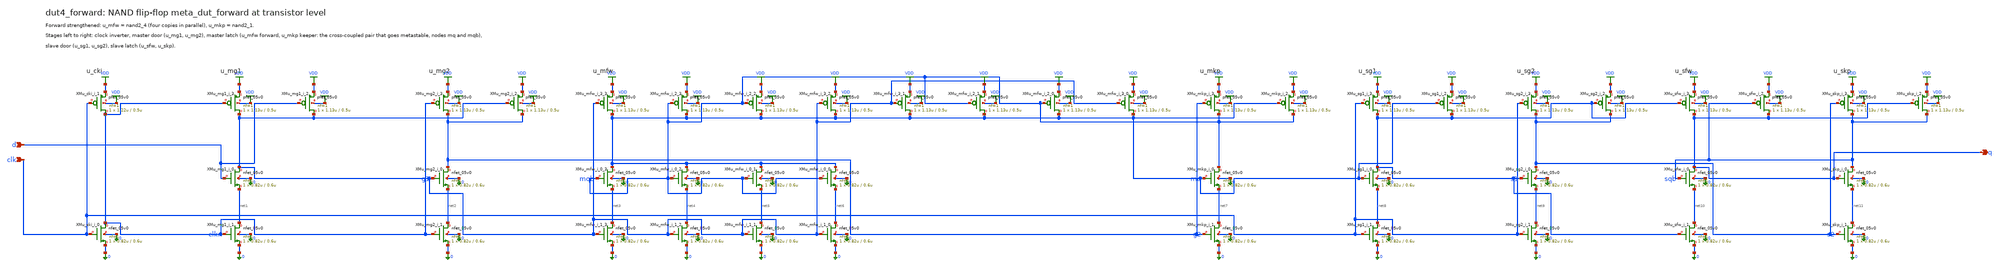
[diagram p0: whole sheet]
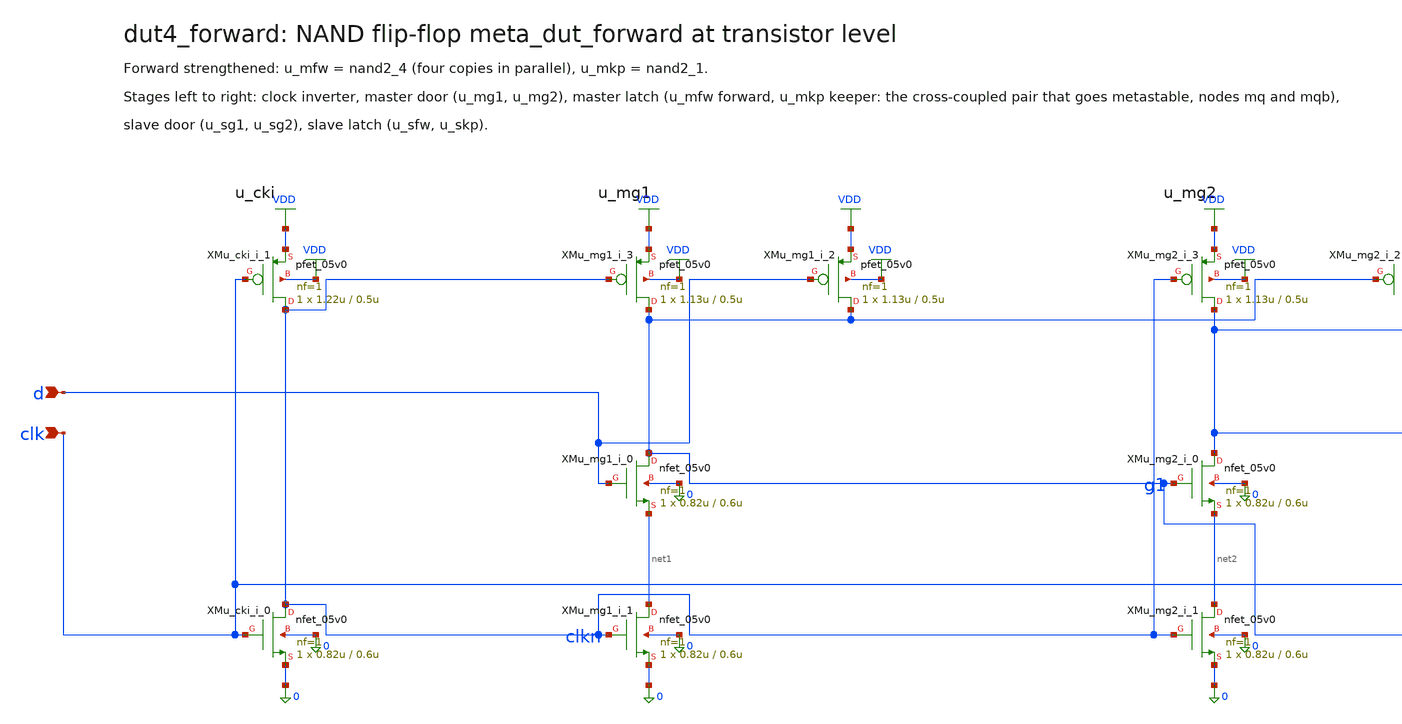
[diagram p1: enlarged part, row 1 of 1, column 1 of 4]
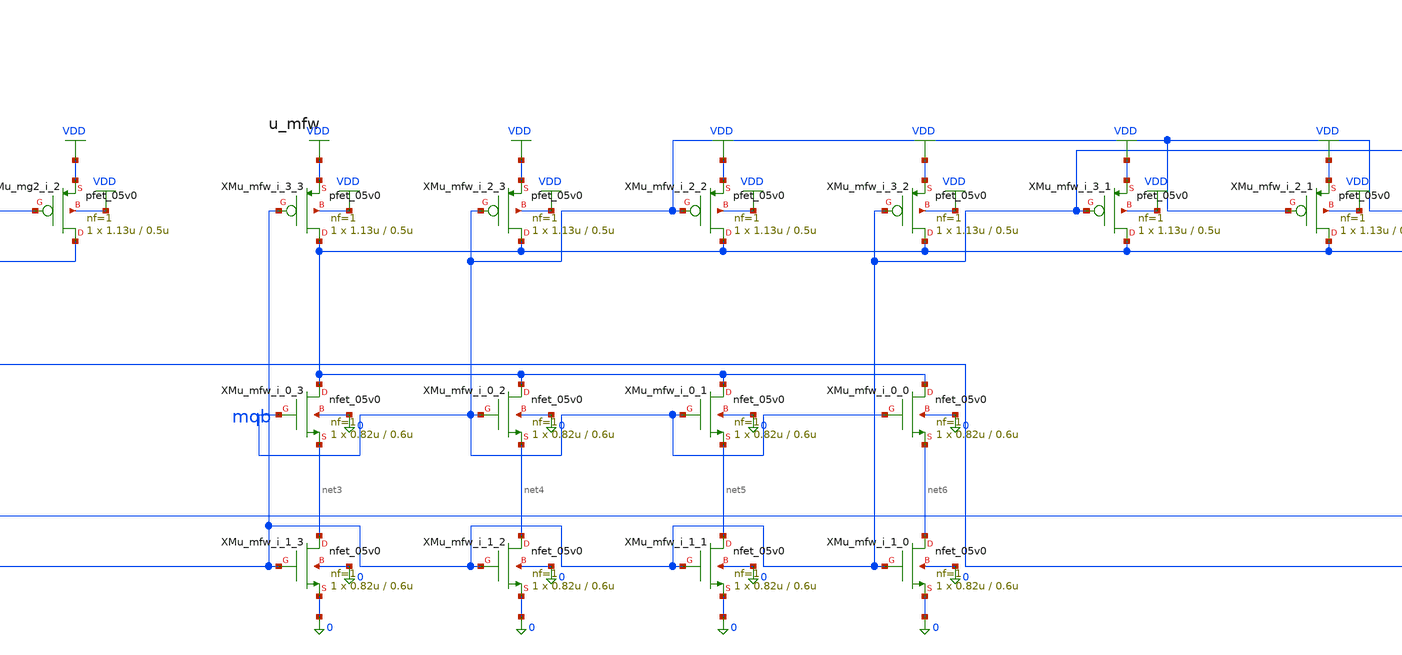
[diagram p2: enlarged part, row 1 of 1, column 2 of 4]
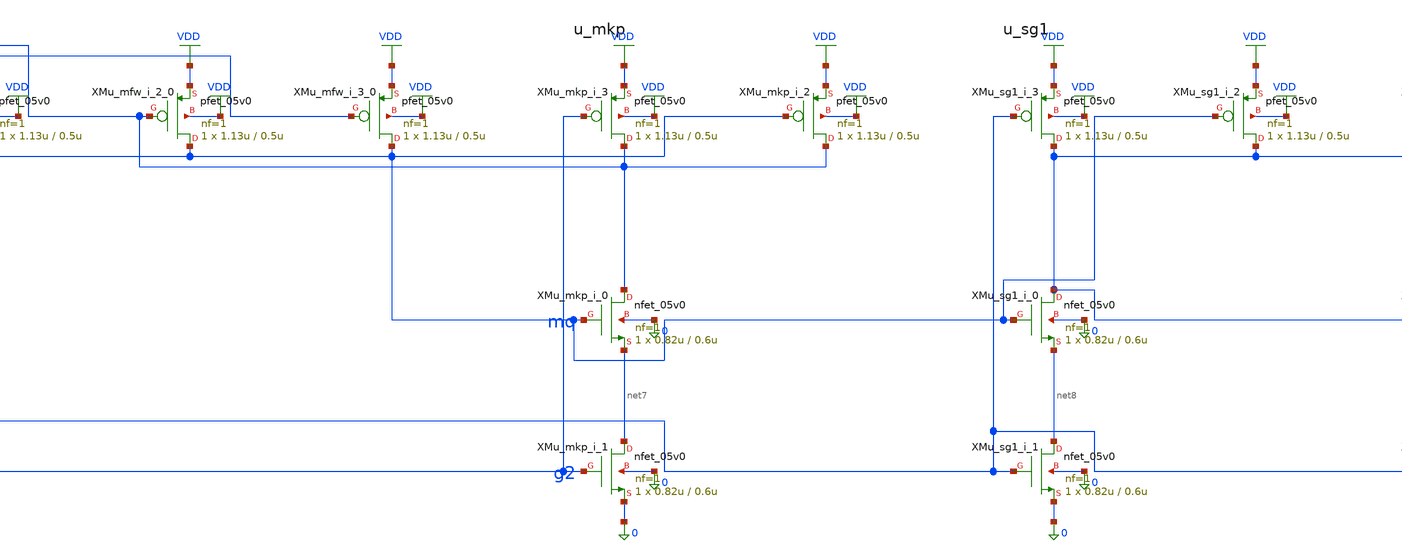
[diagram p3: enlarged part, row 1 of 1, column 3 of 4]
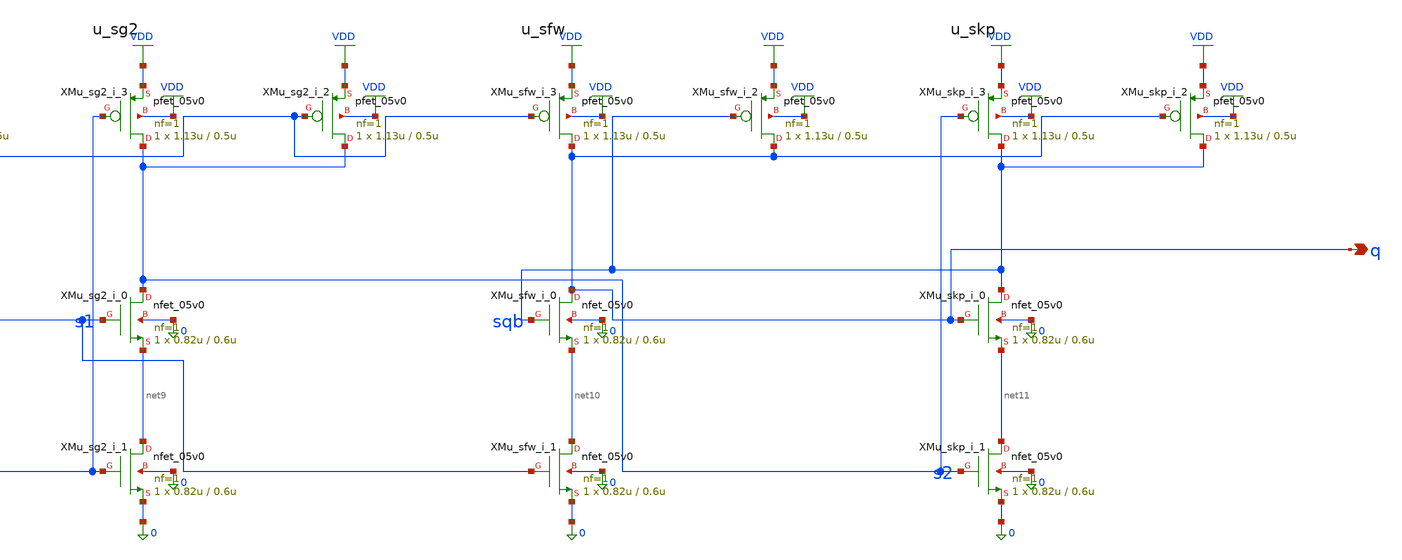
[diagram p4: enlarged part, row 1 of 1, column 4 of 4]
** sch_path: xschem/flat/dut4_forward.sch
**.subckt dut4_forward d clk q
*.ipin d
*.ipin clk
*.opin q
XMu_cki_i_0 clkn clk 0 0 nfet_05v0 L=0.6u W=0.82u nf=1 ad=4.1e-13 as=4.1e-13 pd=2.64e-06 ps=2.64e-06
+ nrd=0 nrs=0 sa=0 sb=0 sd=0 m=1
XMu_cki_i_1 clkn clk VDD VDD pfet_05v0 L=0.5u W=1.22u nf=1 ad=6.1e-13 as=6.1e-13 pd=3.44e-06
+ ps=3.44e-06 nrd=0 nrs=0 sa=0 sb=0 sd=0 m=1
XMu_mg1_i_1 net1 clkn 0 0 nfet_05v0 L=0.6u W=0.82u nf=1 ad=4.1e-13 as=4.1e-13 pd=2.64e-06
+ ps=2.64e-06 nrd=0 nrs=0 sa=0 sb=0 sd=0 m=1
XMu_mg1_i_0 g1 d net1 0 nfet_05v0 L=0.6u W=0.82u nf=1 ad=4.1e-13 as=4.1e-13 pd=2.64e-06 ps=2.64e-06
+ nrd=0 nrs=0 sa=0 sb=0 sd=0 m=1
XMu_mg1_i_3 g1 clkn VDD VDD pfet_05v0 L=0.5u W=1.13u nf=1 ad=5.65e-13 as=5.65e-13 pd=3.26e-06
+ ps=3.26e-06 nrd=0 nrs=0 sa=0 sb=0 sd=0 m=1
XMu_mg1_i_2 g1 d VDD VDD pfet_05v0 L=0.5u W=1.13u nf=1 ad=5.65e-13 as=5.65e-13 pd=3.26e-06
+ ps=3.26e-06 nrd=0 nrs=0 sa=0 sb=0 sd=0 m=1
XMu_mg2_i_1 net2 clkn 0 0 nfet_05v0 L=0.6u W=0.82u nf=1 ad=4.1e-13 as=4.1e-13 pd=2.64e-06
+ ps=2.64e-06 nrd=0 nrs=0 sa=0 sb=0 sd=0 m=1
XMu_mg2_i_0 g2 g1 net2 0 nfet_05v0 L=0.6u W=0.82u nf=1 ad=4.1e-13 as=4.1e-13 pd=2.64e-06 ps=2.64e-06
+ nrd=0 nrs=0 sa=0 sb=0 sd=0 m=1
XMu_mg2_i_3 g2 clkn VDD VDD pfet_05v0 L=0.5u W=1.13u nf=1 ad=5.65e-13 as=5.65e-13 pd=3.26e-06
+ ps=3.26e-06 nrd=0 nrs=0 sa=0 sb=0 sd=0 m=1
XMu_mg2_i_2 g2 g1 VDD VDD pfet_05v0 L=0.5u W=1.13u nf=1 ad=5.65e-13 as=5.65e-13 pd=3.26e-06
+ ps=3.26e-06 nrd=0 nrs=0 sa=0 sb=0 sd=0 m=1
XMu_mfw_i_1_3 net3 g1 0 0 nfet_05v0 L=0.6u W=0.82u nf=1 ad=4.1e-13 as=4.1e-13 pd=2.64e-06
+ ps=2.64e-06 nrd=0 nrs=0 sa=0 sb=0 sd=0 m=1
XMu_mfw_i_0_3 mq mqb net3 0 nfet_05v0 L=0.6u W=0.82u nf=1 ad=4.1e-13 as=4.1e-13 pd=2.64e-06
+ ps=2.64e-06 nrd=0 nrs=0 sa=0 sb=0 sd=0 m=1
XMu_mfw_i_0_2 mq mqb net4 0 nfet_05v0 L=0.6u W=0.82u nf=1 ad=4.1e-13 as=4.1e-13 pd=2.64e-06
+ ps=2.64e-06 nrd=0 nrs=0 sa=0 sb=0 sd=0 m=1
XMu_mfw_i_1_2 net4 g1 0 0 nfet_05v0 L=0.6u W=0.82u nf=1 ad=4.1e-13 as=4.1e-13 pd=2.64e-06
+ ps=2.64e-06 nrd=0 nrs=0 sa=0 sb=0 sd=0 m=1
XMu_mfw_i_1_1 net5 g1 0 0 nfet_05v0 L=0.6u W=0.82u nf=1 ad=4.1e-13 as=4.1e-13 pd=2.64e-06
+ ps=2.64e-06 nrd=0 nrs=0 sa=0 sb=0 sd=0 m=1
XMu_mfw_i_0_1 mq mqb net5 0 nfet_05v0 L=0.6u W=0.82u nf=1 ad=4.1e-13 as=4.1e-13 pd=2.64e-06
+ ps=2.64e-06 nrd=0 nrs=0 sa=0 sb=0 sd=0 m=1
XMu_mfw_i_0_0 mq mqb net6 0 nfet_05v0 L=0.6u W=0.82u nf=1 ad=4.1e-13 as=4.1e-13 pd=2.64e-06
+ ps=2.64e-06 nrd=0 nrs=0 sa=0 sb=0 sd=0 m=1
XMu_mfw_i_1_0 net6 g1 0 0 nfet_05v0 L=0.6u W=0.82u nf=1 ad=4.1e-13 as=4.1e-13 pd=2.64e-06
+ ps=2.64e-06 nrd=0 nrs=0 sa=0 sb=0 sd=0 m=1
XMu_mfw_i_3_3 mq g1 VDD VDD pfet_05v0 L=0.5u W=1.13u nf=1 ad=5.65e-13 as=5.65e-13 pd=3.26e-06
+ ps=3.26e-06 nrd=0 nrs=0 sa=0 sb=0 sd=0 m=1
XMu_mfw_i_2_3 mq mqb VDD VDD pfet_05v0 L=0.5u W=1.13u nf=1 ad=5.65e-13 as=5.65e-13 pd=3.26e-06
+ ps=3.26e-06 nrd=0 nrs=0 sa=0 sb=0 sd=0 m=1
XMu_mfw_i_2_2 mq mqb VDD VDD pfet_05v0 L=0.5u W=1.13u nf=1 ad=5.65e-13 as=5.65e-13 pd=3.26e-06
+ ps=3.26e-06 nrd=0 nrs=0 sa=0 sb=0 sd=0 m=1
XMu_mfw_i_3_2 mq g1 VDD VDD pfet_05v0 L=0.5u W=1.13u nf=1 ad=5.65e-13 as=5.65e-13 pd=3.26e-06
+ ps=3.26e-06 nrd=0 nrs=0 sa=0 sb=0 sd=0 m=1
XMu_mfw_i_3_1 mq g1 VDD VDD pfet_05v0 L=0.5u W=1.13u nf=1 ad=5.65e-13 as=5.65e-13 pd=3.26e-06
+ ps=3.26e-06 nrd=0 nrs=0 sa=0 sb=0 sd=0 m=1
XMu_mfw_i_2_1 mq mqb VDD VDD pfet_05v0 L=0.5u W=1.13u nf=1 ad=5.65e-13 as=5.65e-13 pd=3.26e-06
+ ps=3.26e-06 nrd=0 nrs=0 sa=0 sb=0 sd=0 m=1
XMu_mfw_i_2_0 mq mqb VDD VDD pfet_05v0 L=0.5u W=1.13u nf=1 ad=5.65e-13 as=5.65e-13 pd=3.26e-06
+ ps=3.26e-06 nrd=0 nrs=0 sa=0 sb=0 sd=0 m=1
XMu_mfw_i_3_0 mq g1 VDD VDD pfet_05v0 L=0.5u W=1.13u nf=1 ad=5.65e-13 as=5.65e-13 pd=3.26e-06
+ ps=3.26e-06 nrd=0 nrs=0 sa=0 sb=0 sd=0 m=1
XMu_mkp_i_1 net7 g2 0 0 nfet_05v0 L=0.6u W=0.82u nf=1 ad=4.1e-13 as=4.1e-13 pd=2.64e-06 ps=2.64e-06
+ nrd=0 nrs=0 sa=0 sb=0 sd=0 m=1
XMu_mkp_i_0 mqb mq net7 0 nfet_05v0 L=0.6u W=0.82u nf=1 ad=4.1e-13 as=4.1e-13 pd=2.64e-06
+ ps=2.64e-06 nrd=0 nrs=0 sa=0 sb=0 sd=0 m=1
XMu_mkp_i_3 mqb g2 VDD VDD pfet_05v0 L=0.5u W=1.13u nf=1 ad=5.65e-13 as=5.65e-13 pd=3.26e-06
+ ps=3.26e-06 nrd=0 nrs=0 sa=0 sb=0 sd=0 m=1
XMu_mkp_i_2 mqb mq VDD VDD pfet_05v0 L=0.5u W=1.13u nf=1 ad=5.65e-13 as=5.65e-13 pd=3.26e-06
+ ps=3.26e-06 nrd=0 nrs=0 sa=0 sb=0 sd=0 m=1
XMu_sg1_i_1 net8 clk 0 0 nfet_05v0 L=0.6u W=0.82u nf=1 ad=4.1e-13 as=4.1e-13 pd=2.64e-06 ps=2.64e-06
+ nrd=0 nrs=0 sa=0 sb=0 sd=0 m=1
XMu_sg1_i_0 s1 mq net8 0 nfet_05v0 L=0.6u W=0.82u nf=1 ad=4.1e-13 as=4.1e-13 pd=2.64e-06 ps=2.64e-06
+ nrd=0 nrs=0 sa=0 sb=0 sd=0 m=1
XMu_sg1_i_3 s1 clk VDD VDD pfet_05v0 L=0.5u W=1.13u nf=1 ad=5.65e-13 as=5.65e-13 pd=3.26e-06
+ ps=3.26e-06 nrd=0 nrs=0 sa=0 sb=0 sd=0 m=1
XMu_sg1_i_2 s1 mq VDD VDD pfet_05v0 L=0.5u W=1.13u nf=1 ad=5.65e-13 as=5.65e-13 pd=3.26e-06
+ ps=3.26e-06 nrd=0 nrs=0 sa=0 sb=0 sd=0 m=1
XMu_sg2_i_1 net9 clk 0 0 nfet_05v0 L=0.6u W=0.82u nf=1 ad=4.1e-13 as=4.1e-13 pd=2.64e-06 ps=2.64e-06
+ nrd=0 nrs=0 sa=0 sb=0 sd=0 m=1
XMu_sg2_i_0 s2 s1 net9 0 nfet_05v0 L=0.6u W=0.82u nf=1 ad=4.1e-13 as=4.1e-13 pd=2.64e-06 ps=2.64e-06
+ nrd=0 nrs=0 sa=0 sb=0 sd=0 m=1
XMu_sg2_i_3 s2 clk VDD VDD pfet_05v0 L=0.5u W=1.13u nf=1 ad=5.65e-13 as=5.65e-13 pd=3.26e-06
+ ps=3.26e-06 nrd=0 nrs=0 sa=0 sb=0 sd=0 m=1
XMu_sg2_i_2 s2 s1 VDD VDD pfet_05v0 L=0.5u W=1.13u nf=1 ad=5.65e-13 as=5.65e-13 pd=3.26e-06
+ ps=3.26e-06 nrd=0 nrs=0 sa=0 sb=0 sd=0 m=1
XMu_sfw_i_1 net10 s1 0 0 nfet_05v0 L=0.6u W=0.82u nf=1 ad=4.1e-13 as=4.1e-13 pd=2.64e-06 ps=2.64e-06
+ nrd=0 nrs=0 sa=0 sb=0 sd=0 m=1
XMu_sfw_i_0 q sqb net10 0 nfet_05v0 L=0.6u W=0.82u nf=1 ad=4.1e-13 as=4.1e-13 pd=2.64e-06
+ ps=2.64e-06 nrd=0 nrs=0 sa=0 sb=0 sd=0 m=1
XMu_sfw_i_3 q s1 VDD VDD pfet_05v0 L=0.5u W=1.13u nf=1 ad=5.65e-13 as=5.65e-13 pd=3.26e-06
+ ps=3.26e-06 nrd=0 nrs=0 sa=0 sb=0 sd=0 m=1
XMu_sfw_i_2 q sqb VDD VDD pfet_05v0 L=0.5u W=1.13u nf=1 ad=5.65e-13 as=5.65e-13 pd=3.26e-06
+ ps=3.26e-06 nrd=0 nrs=0 sa=0 sb=0 sd=0 m=1
XMu_skp_i_1 net11 s2 0 0 nfet_05v0 L=0.6u W=0.82u nf=1 ad=4.1e-13 as=4.1e-13 pd=2.64e-06 ps=2.64e-06
+ nrd=0 nrs=0 sa=0 sb=0 sd=0 m=1
XMu_skp_i_0 sqb q net11 0 nfet_05v0 L=0.6u W=0.82u nf=1 ad=4.1e-13 as=4.1e-13 pd=2.64e-06
+ ps=2.64e-06 nrd=0 nrs=0 sa=0 sb=0 sd=0 m=1
XMu_skp_i_3 sqb s2 VDD VDD pfet_05v0 L=0.5u W=1.13u nf=1 ad=5.65e-13 as=5.65e-13 pd=3.26e-06
+ ps=3.26e-06 nrd=0 nrs=0 sa=0 sb=0 sd=0 m=1
XMu_skp_i_2 sqb q VDD VDD pfet_05v0 L=0.5u W=1.13u nf=1 ad=5.65e-13 as=5.65e-13 pd=3.26e-06
+ ps=3.26e-06 nrd=0 nrs=0 sa=0 sb=0 sd=0 m=1
**.ends
.GLOBAL VDD
.end
